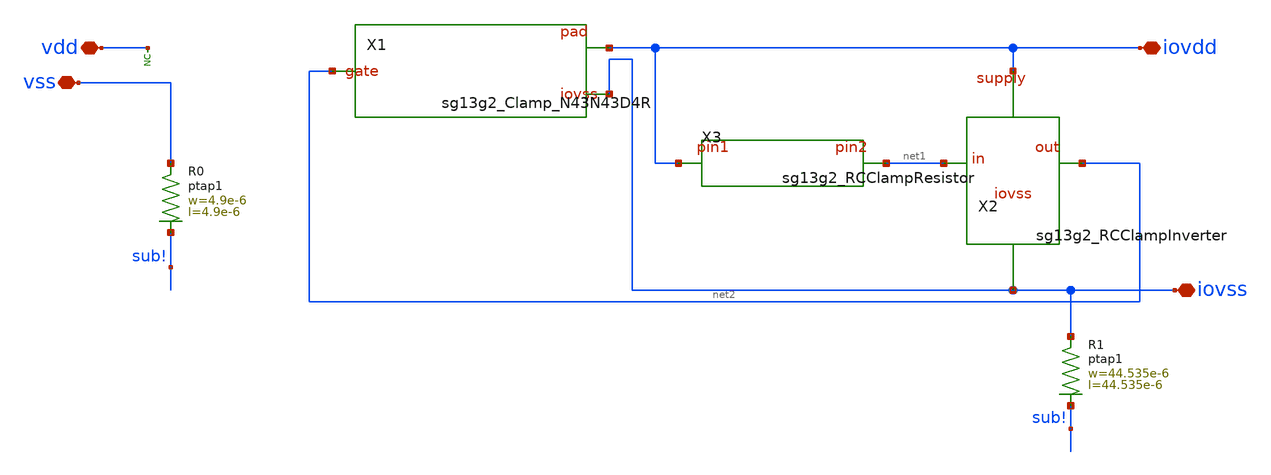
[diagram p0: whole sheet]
** sch_path: ihp-sg13g2/libs.ref/sg13g2_io/sch/xschem/sg13g2_IOPadIOVdd.sch
**.subckt sg13g2_IOPadIOVdd iovdd vdd iovss vss
*.iopin iovdd
*.iopin vdd
*.iopin iovss
*.iopin vss
* noconn vdd
X1 net2 iovss iovdd sg13g2_Clamp_N43N43D4R
X2 iovdd net2 net1 iovss sg13g2_RCClampInverter
X3 net1 iovdd sg13g2_RCClampResistor
XR0 vss sub! ptap1 R=22.47 w=4.9e-6 l=4.9e-6
XR1 iovss sub! ptap1 R=453.4m w=44.535e-6 l=44.535e-6
**.ends
.end
